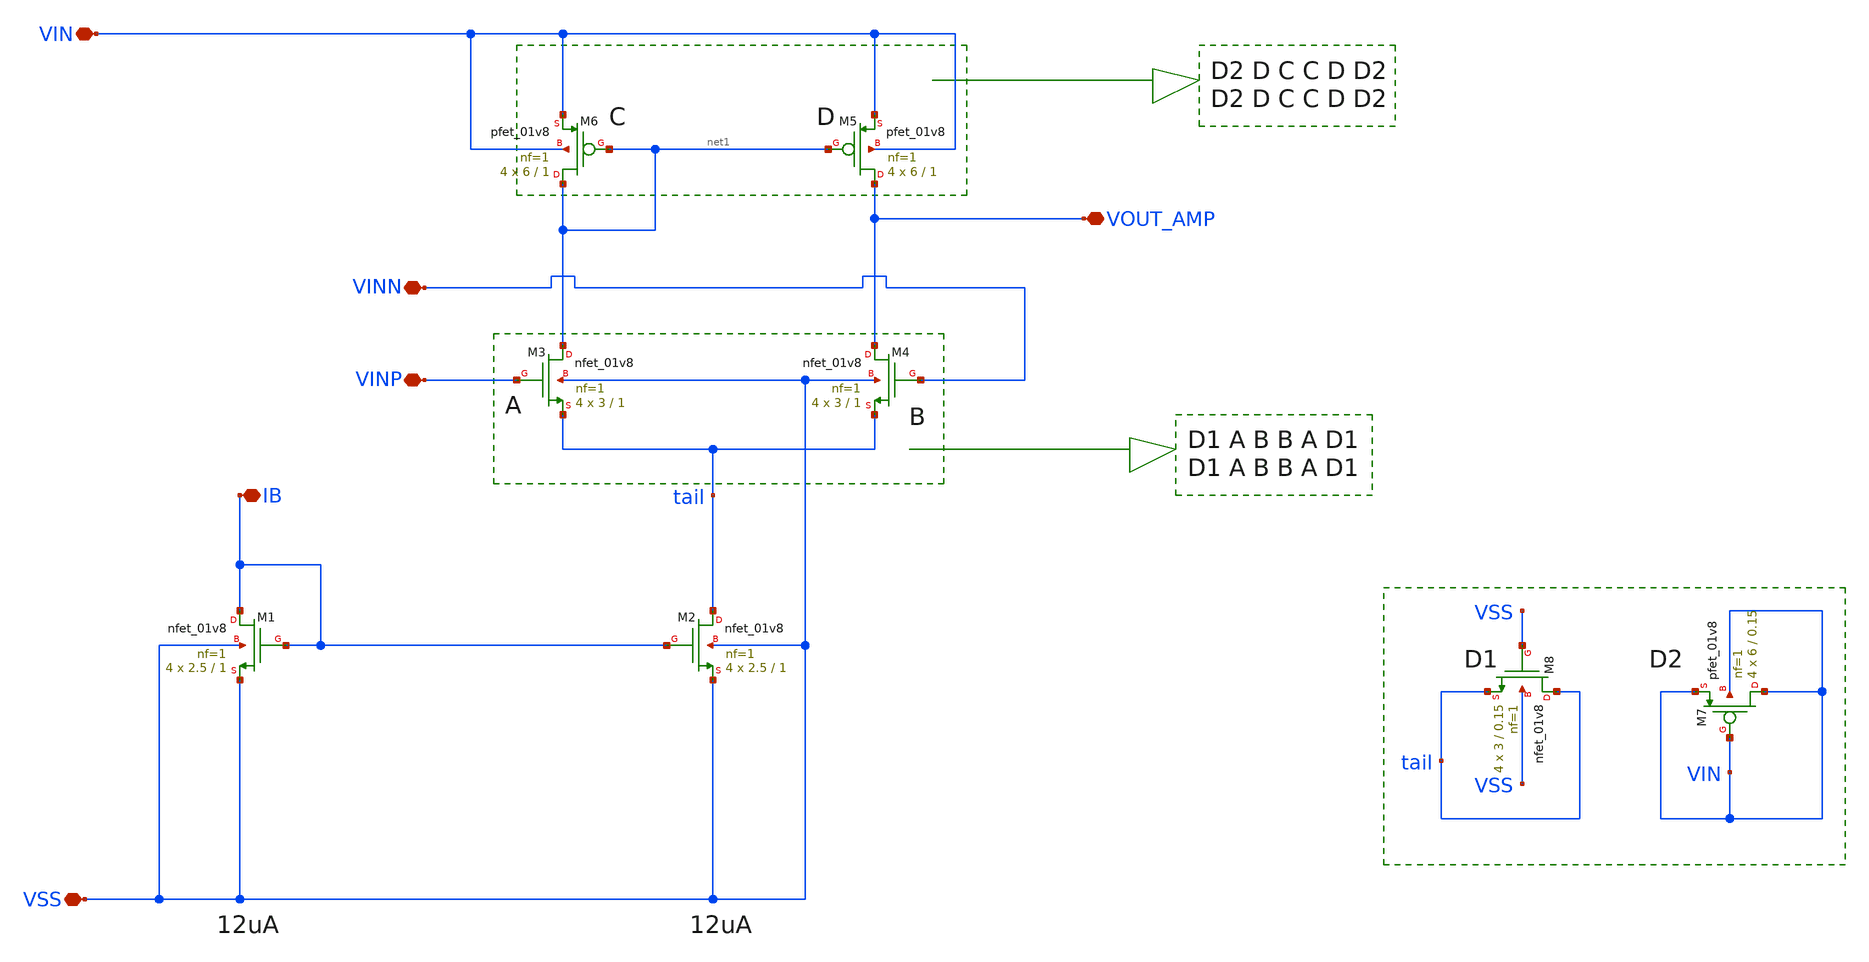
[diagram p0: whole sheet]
** sch_path: common/analog/ota5t/OTA_5T.sch
**.subckt OTA_5T VIN VSS VOUT_AMP IB VINN VINP
*.iopin VIN
*.iopin VSS
*.iopin VOUT_AMP
*.iopin IB
*.iopin VINN
*.iopin VINP
XM1 IB IB VSS VSS sky130_fd_pr__nfet_01v8 L=1 W=2.5 nf=1 ad='int((1 + 1)/2) * 2.5 / 1 * 0.29' as='int((1 + 2)/2) * 2.5 / 1 * 0.29'
+ pd='2*int((1 + 1)/2) * (2.5 / 1 + 0.29)' ps='2*int((1 + 2)/2) * (2.5 / 1 + 0.29)' nrd='0.29 / 2.5 ' nrs='0.29 / 2.5 '
+ sa=0 sb=0 sd=0 mult=4 m=4
XM2 tail IB VSS VSS sky130_fd_pr__nfet_01v8 L=1 W=2.5 nf=1 ad='int((1 + 1)/2) * 2.5 / 1 * 0.29' as='int((1 + 2)/2) * 2.5 / 1 * 0.29'
+ pd='2*int((1 + 1)/2) * (2.5 / 1 + 0.29)' ps='2*int((1 + 2)/2) * (2.5 / 1 + 0.29)' nrd='0.29 / 2.5 ' nrs='0.29 / 2.5 '
+ sa=0 sb=0 sd=0 mult=4 m=4
XM3 net1 VINP tail VSS sky130_fd_pr__nfet_01v8 L=1 W=3 nf=1 ad='int((1 + 1)/2) * 3 / 1 * 0.29' as='int((1 + 2)/2) * 3 / 1 * 0.29'
+ pd='2*int((1 + 1)/2) * (3 / 1 + 0.29)' ps='2*int((1 + 2)/2) * (3 / 1 + 0.29)' nrd='0.29 / 3 ' nrs='0.29 / 3 '
+ sa=0 sb=0 sd=0 mult=4 m=4
XM4 VOUT_AMP VINN tail VSS sky130_fd_pr__nfet_01v8 L=1 W=3 nf=1 ad='int((1 + 1)/2) * 3 / 1 * 0.29' as='int((1 + 2)/2) * 3 / 1 * 0.29'
+ pd='2*int((1 + 1)/2) * (3 / 1 + 0.29)' ps='2*int((1 + 2)/2) * (3 / 1 + 0.29)' nrd='0.29 / 3 ' nrs='0.29 / 3 '
+ sa=0 sb=0 sd=0 mult=4 m=4
XM5 VOUT_AMP net1 VIN VIN sky130_fd_pr__pfet_01v8 L=1 W=6 nf=1 ad='int((1 + 1)/2) * 6 / 1 * 0.29' as='int((1 + 2)/2) * 6 / 1 * 0.29'
+ pd='2*int((1 + 1)/2) * (6 / 1 + 0.29)' ps='2*int((1 + 2)/2) * (6 / 1 + 0.29)' nrd='0.29 / 6 ' nrs='0.29 / 6 '
+ sa=0 sb=0 sd=0 mult=4 m=4
XM6 net1 net1 VIN VIN sky130_fd_pr__pfet_01v8 L=1 W=6 nf=1 ad='int((1 + 1)/2) * 6 / 1 * 0.29' as='int((1 + 2)/2) * 6 / 1 * 0.29'
+ pd='2*int((1 + 1)/2) * (6 / 1 + 0.29)' ps='2*int((1 + 2)/2) * (6 / 1 + 0.29)' nrd='0.29 / 6 ' nrs='0.29 / 6 '
+ sa=0 sb=0 sd=0 mult=4 m=4
XM8 tail VSS tail VSS sky130_fd_pr__nfet_01v8 L=0.15 W=3 nf=1 ad='int((1 + 1)/2) * 3 / 1 * 0.29' as='int((1 + 2)/2) * 3 / 1 * 0.29'
+ pd='2*int((1 + 1)/2) * (3 / 1 + 0.29)' ps='2*int((1 + 2)/2) * (3 / 1 + 0.29)' nrd='0.29 / 3 ' nrs='0.29 / 3 '
+ sa=0 sb=0 sd=0 mult=4 m=4
XM7 VIN VIN VIN VIN sky130_fd_pr__pfet_01v8 L=0.15 W=6 nf=1 ad='int((1 + 1)/2) * 6 / 1 * 0.29' as='int((1 + 2)/2) * 6 / 1 * 0.29'
+ pd='2*int((1 + 1)/2) * (6 / 1 + 0.29)' ps='2*int((1 + 2)/2) * (6 / 1 + 0.29)' nrd='0.29 / 6 ' nrs='0.29 / 6 '
+ sa=0 sb=0 sd=0 mult=4 m=4
**.ends
.end
